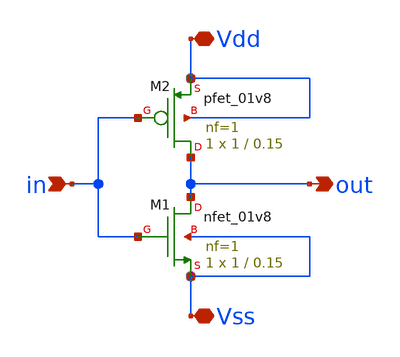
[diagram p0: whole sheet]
** sch_path: sandbox/inv-experimental/inv.sch
**.subckt inv in Vdd out Vss
*.ipin in
*.iopin Vdd
*.opin out
*.iopin Vss
XM1 out in Vss Vss sky130_fd_pr__nfet_01v8 L=0.15 W=1 nf=1 ad='int((1 + 1)/2) * 1 / 1 * 0.29' as='int((1 + 2)/2) * 1 / 1 * 0.29'
+ pd='2*int((1 + 1)/2) * (1 / 1 + 0.29)' ps='2*int((1 + 2)/2) * (1 / 1 + 0.29)' nrd='0.29 / 1 ' nrs='0.29 / 1 '
+ sa=0 sb=0 sd=0 mult=1 m=1
XM2 out in Vdd Vdd sky130_fd_pr__pfet_01v8 L=0.15 W=1 nf=1 ad='int((1 + 1)/2) * 1 / 1 * 0.29' as='int((1 + 2)/2) * 1 / 1 * 0.29'
+ pd='2*int((1 + 1)/2) * (1 / 1 + 0.29)' ps='2*int((1 + 2)/2) * (1 / 1 + 0.29)' nrd='0.29 / 1 ' nrs='0.29 / 1 '
+ sa=0 sb=0 sd=0 mult=1 m=1
**.ends
.end
